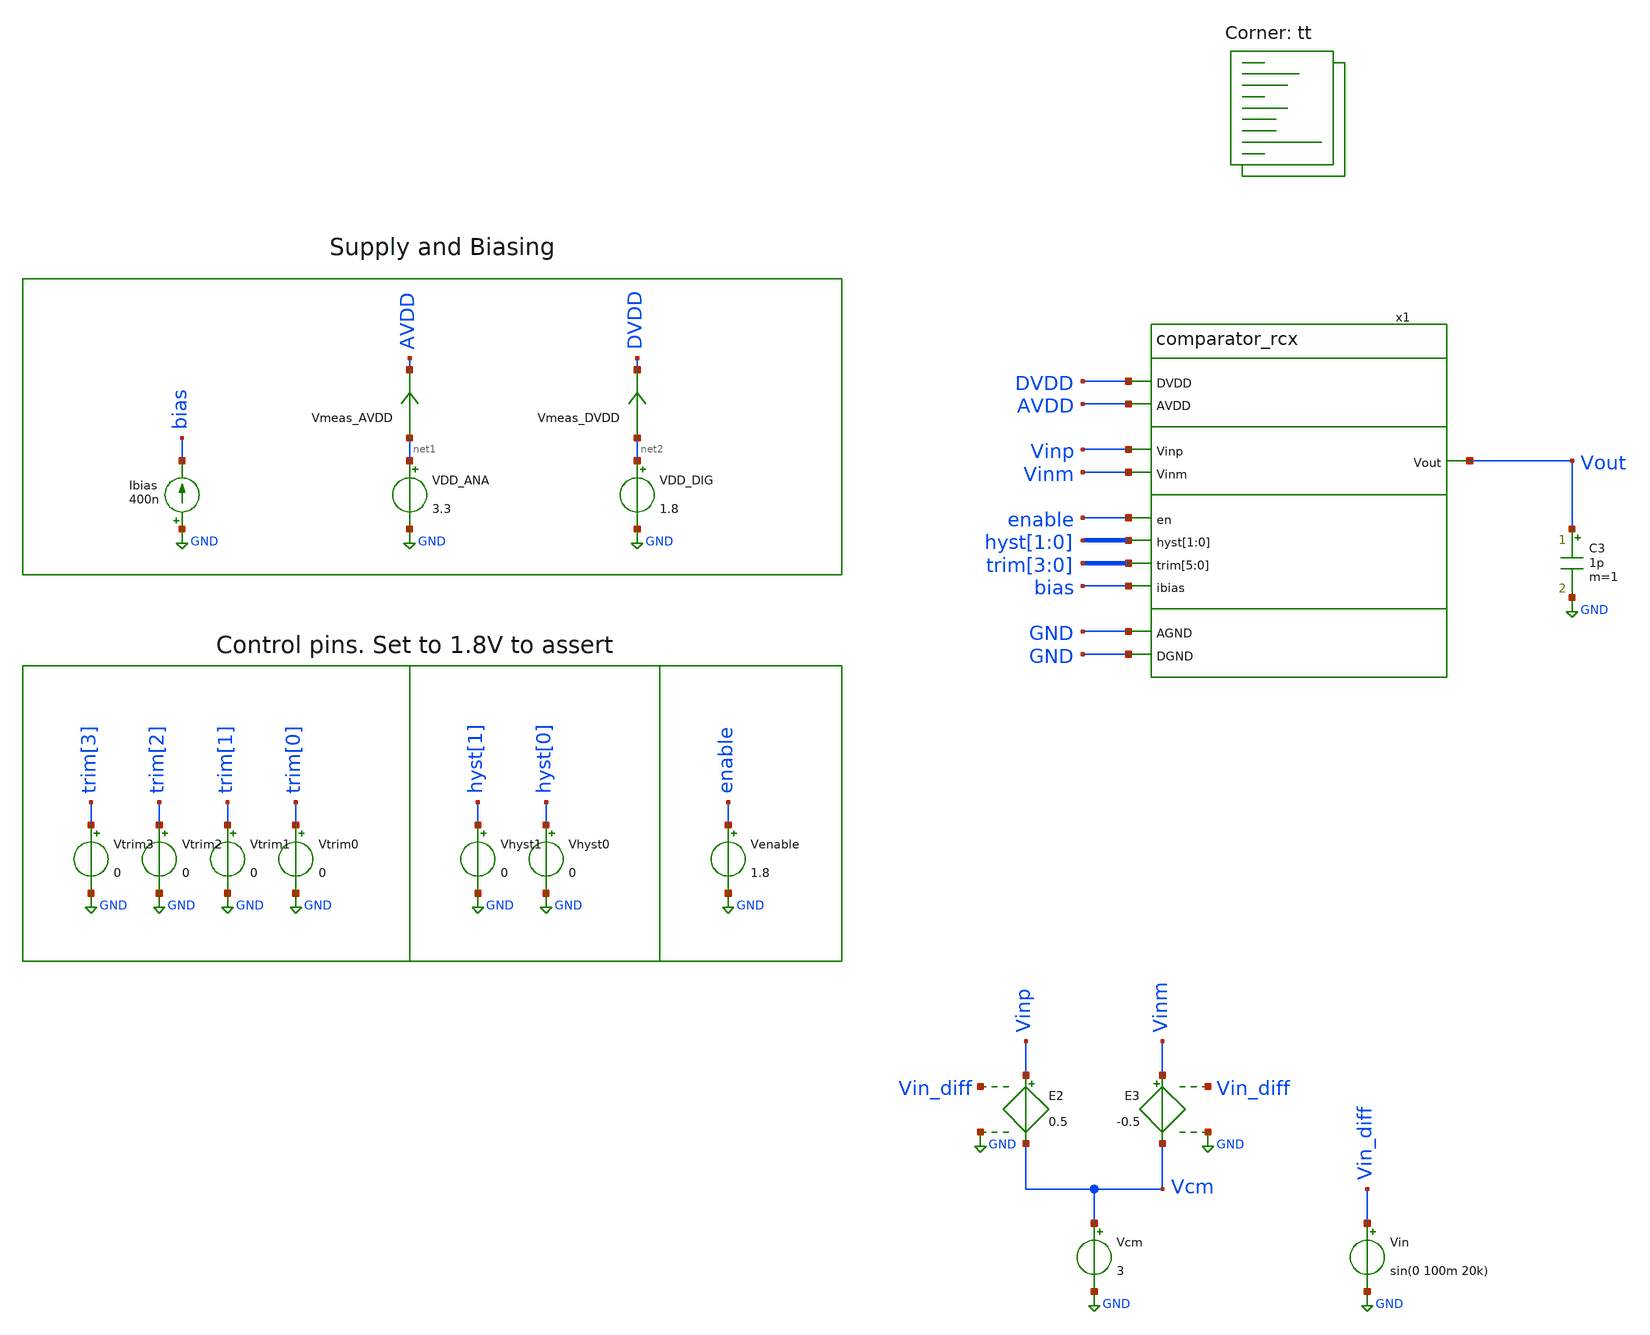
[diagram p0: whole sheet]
** sch_path: xschem/tb_comparator.sch
**.subckt tb_comparator
Vtrim3 trim[3] GND 0
VDD_ANA net1 GND 3.3
VDD_DIG net2 GND 1.8
Ibias GND bias 400n
C3 Vout GND 1p m=1
Vtrim2 trim[2] GND 0
Vtrim1 trim[1] GND 0
Vtrim0 trim[0] GND 0
Vhyst1 hyst[1] GND 0
Vhyst0 hyst[0] GND 0
Venable enable GND 1.8
Vmeas_AVDD net1 AVDD 0
.save i(vmeas_avdd)
Vmeas_DVDD net2 DVDD 0
.save i(vmeas_dvdd)
Vcm Vcm GND 3
Vin Vin_diff GND sin(0 100m 20k)
E2 Vinp Vcm Vin_diff GND 0.5
E3 Vinm Vcm Vin_diff GND -0.5
x1 DVDD AVDD GND Vinp Vout Vinm enable hyst[1] hyst[0] trim[3] trim[2] trim[1] trim[0] trim[3]
+ trim[2] bias GND comparator_rcx
**** begin user architecture code
.lib $::SKYWATER_MODELS/sky130.lib.spice tt


.include /foss/designs/sky130_ak_ip__comparator/mag/comparator_rcx.spice
.save v(vout) v(vin_diff)
.tran 3n 100u
.temp 25
.control
   run
   plot v(vout)
   plot v(vin_diff)
   *plot v.x1.vmeas1#branch v.x1.vmeas6#branch v.x1.vmeas2#branch
   *plot v.x1.vmeas4#branch
   *plot v.x1.vmeas9#branch v.x1.vmeas10#branch v.x1.vmeas11#branch v.x1.vmeas12#branch
   *plot v.x1.vmeas20#branch v.x1.vmeas21#branch
   *plot v(x1.vfold_m) v(x1.vxm)
   *plot v(x1.bias_p) v(x1.casc_p) v(x1.test) v(x1.casc_n) v(x1.bias_n)
.endc


**** end user architecture code
**.ends
.GLOBAL GND
.end
